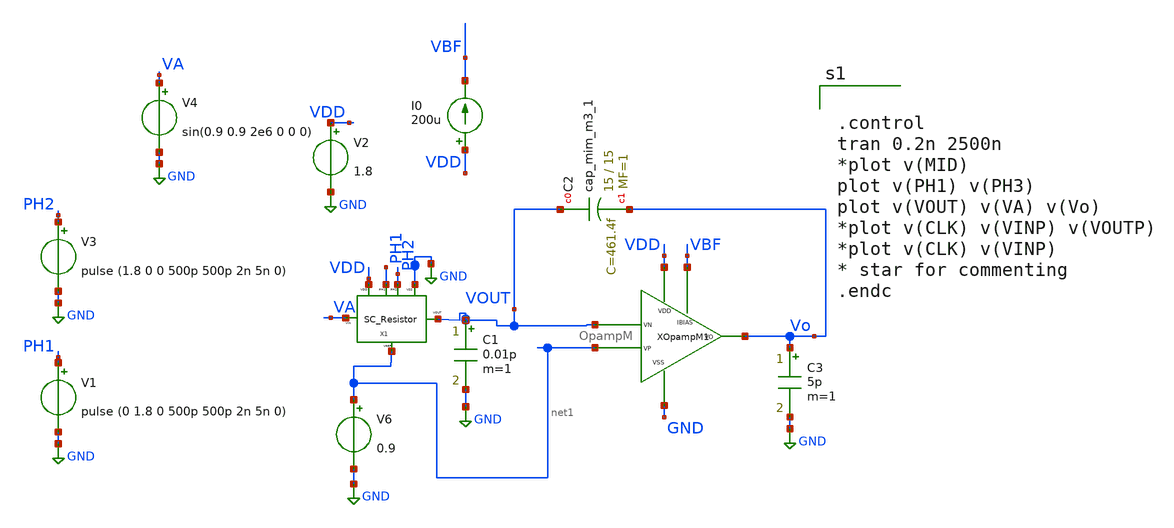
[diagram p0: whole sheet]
** sch_path: xschem/xschem_BGR_Top/Sigma_Delta/Integrator/Integrator_TB_rough.sch
**.subckt Integrator_TB_rough
V1 PH1 GND pulse (0 1.8 0 500p 500p 2n 5n 0)
V2 VDD GND 1.8
V3 PH2 GND pulse (1.8 0 0 500p 500p 2n 5n 0)
V6 net1 GND 0.9
C1 VOUT GND 0.01p m=1
X1 net1 PH2 VOUT VDD GND PH1 VA SC_Resistor
XOpampM1 VBF VDD VOUT net1 GND Vo OpampM
XC2 VOUT Vo sky130_fd_pr__cap_mim_m3_1 W=15 L=15 MF=1 m=1
I0 VDD VBF 200u
C3 Vo GND 5p m=1
V4 VA GND sin(0.9 0.9 2e6 0 0 0)
**** begin user architecture code


.control
tran 0.2n 2500n
*plot v(MID)
plot v(PH1) v(PH3)
plot v(VOUT) v(VA) v(Vo)
*plot v(CLK) v(VINP) v(VOUTP)
*plot v(CLK) v(VINP)
* star for commenting
.endc


** opencircuitdesign pdks install
.lib $::SKYWATER_MODELS/sky130.lib.spice tt


**** end user architecture code
**.ends

* expanding   symbol:  Sigma_Delta/SC_Resistor/SC_Resistor.sym # of pins=7
** sym_path: xschem/xschem_BGR_Top/Sigma_Delta/SC_Resistor/SC_Resistor.sym
** sch_path: xschem/xschem_BGR_Top/Sigma_Delta/SC_Resistor/SC_Resistor.sch
.subckt SC_Resistor VREF PH2 VOUT VDD VSS PH1 VIN
*.iopin VDD
*.iopin PH1
*.iopin VIN
*.iopin VOUT
*.iopin PH2
*.iopin VREF
*.iopin VSS
XTG3 VSS PH1 VDD VIN MID1 TG
XTG4 VSS PH2 VDD MID2 VOUT TG
XM2 MID1 PH2 VREF VSS sky130_fd_pr__nfet_01v8 L=0.15 W=20 nf=2 ad='int((nf+1)/2) * W/nf * 0.29' as='int((nf+2)/2) * W/nf * 0.29'
+ pd='2*int((nf+1)/2) * (W/nf + 0.29)' ps='2*int((nf+2)/2) * (W/nf + 0.29)' nrd='0.29 / W' nrs='0.29 / W'
+ sa=0 sb=0 sd=0 mult=1 m=1
XM1 MID2 PH1 VREF VSS sky130_fd_pr__nfet_01v8 L=0.15 W=20 nf=2 ad='int((nf+1)/2) * W/nf * 0.29' as='int((nf+2)/2) * W/nf * 0.29'
+ pd='2*int((nf+1)/2) * (W/nf + 0.29)' ps='2*int((nf+2)/2) * (W/nf + 0.29)' nrd='0.29 / W' nrs='0.29 / W'
+ sa=0 sb=0 sd=0 mult=1 m=1
XC2 MID2 MID1 sky130_fd_pr__cap_mim_m3_2 W=32 L=32 MF=1 m=1
.ends


* expanding   symbol:  Sigma_Delta/Op_Amp/OpampM.sym # of pins=6
** sym_path: xschem/xschem_BGR_Top/Op_Amp/OpampM.sym
** sch_path: xschem/xschem_BGR_Top/Op_Amp/OpampM.sch
.subckt OpampM IBIAS VDD VN VP VSS VO
*.iopin VDD
*.iopin VSS
*.iopin VP
*.iopin VN
*.iopin VO
*.iopin IBIAS
XM1 net1 VN net3 VSS sky130_fd_pr__nfet_01v8 L=0.5 W=50 nf=10 ad='int((nf+1)/2) * W/nf * 0.29' as='int((nf+2)/2) * W/nf * 0.29'
+ pd='2*int((nf+1)/2) * (W/nf + 0.29)' ps='2*int((nf+2)/2) * (W/nf + 0.29)' nrd='0.29 / W' nrs='0.29 / W'
+ sa=0 sb=0 sd=0 mult=1 m=1
XM3 net1 net1 VDD VDD sky130_fd_pr__pfet_01v8_lvt L=0.5 W=60 nf=10 ad='int((nf+1)/2) * W/nf * 0.29' as='int((nf+2)/2) * W/nf * 0.29'
+ pd='2*int((nf+1)/2) * (W/nf + 0.29)' ps='2*int((nf+2)/2) * (W/nf + 0.29)' nrd='0.29 / W' nrs='0.29 / W'
+ sa=0 sb=0 sd=0 mult=1 m=1
XM2 net2 VP net3 VSS sky130_fd_pr__nfet_01v8 L=0.5 W=50 nf=10 ad='int((nf+1)/2) * W/nf * 0.29' as='int((nf+2)/2) * W/nf * 0.29'
+ pd='2*int((nf+1)/2) * (W/nf + 0.29)' ps='2*int((nf+2)/2) * (W/nf + 0.29)' nrd='0.29 / W' nrs='0.29 / W'
+ sa=0 sb=0 sd=0 mult=1 m=1
XM4 net2 net1 VDD VDD sky130_fd_pr__pfet_01v8_lvt L=0.5 W=60 nf=10 ad='int((nf+1)/2) * W/nf * 0.29' as='int((nf+2)/2) * W/nf * 0.29'
+ pd='2*int((nf+1)/2) * (W/nf + 0.29)' ps='2*int((nf+2)/2) * (W/nf + 0.29)' nrd='0.29 / W' nrs='0.29 / W'
+ sa=0 sb=0 sd=0 mult=1 m=1
XM5 net3 IBIAS VSS VSS sky130_fd_pr__nfet_01v8 L=0.5 W=21 nf=10 ad='int((nf+1)/2) * W/nf * 0.29' as='int((nf+2)/2) * W/nf * 0.29'
+ pd='2*int((nf+1)/2) * (W/nf + 0.29)' ps='2*int((nf+2)/2) * (W/nf + 0.29)' nrd='0.29 / W' nrs='0.29 / W'
+ sa=0 sb=0 sd=0 mult=1 m=1
XM7 VO IBIAS VSS VSS sky130_fd_pr__nfet_01v8 L=0.5 W=63 nf=10 ad='int((nf+1)/2) * W/nf * 0.29' as='int((nf+2)/2) * W/nf * 0.29'
+ pd='2*int((nf+1)/2) * (W/nf + 0.29)' ps='2*int((nf+2)/2) * (W/nf + 0.29)' nrd='0.29 / W' nrs='0.29 / W'
+ sa=0 sb=0 sd=0 mult=1 m=1
XM8 IBIAS IBIAS VSS VSS sky130_fd_pr__nfet_01v8 L=0.5 W=21 nf=10 ad='int((nf+1)/2) * W/nf * 0.29' as='int((nf+2)/2) * W/nf * 0.29'
+ pd='2*int((nf+1)/2) * (W/nf + 0.29)' ps='2*int((nf+2)/2) * (W/nf + 0.29)' nrd='0.29 / W' nrs='0.29 / W'
+ sa=0 sb=0 sd=0 mult=1 m=1
XC1 net2 VO sky130_fd_pr__cap_mim_m3_1 W=24 L=24 MF=1 m=1
XC2 VDD VSS sky130_fd_pr__cap_mim_m3_1 W=30 L=10 MF=1 m=1
XC3 VDD VSS sky130_fd_pr__cap_mim_m3_1 W=30 L=10 MF=1 m=1
XM6 VO net2 VDD VDD sky130_fd_pr__pfet_01v8_lvt L=0.50 W=355 nf=20 ad='int((nf+1)/2) * W/nf * 0.29' as='int((nf+2)/2) * W/nf * 0.29'
+ pd='2*int((nf+1)/2) * (W/nf + 0.29)' ps='2*int((nf+2)/2) * (W/nf + 0.29)' nrd='0.29 / W' nrs='0.29 / W'
+ sa=0 sb=0 sd=0 mult=1 m=1
.ends


* expanding   symbol:  Sigma_Delta/Transmission_Gate/TG.sym # of pins=5
** sym_path: xschem/xschem_BGR_Top/Sigma_Delta/Transmission_Gate/TG.sym
** sch_path: xschem/xschem_BGR_Top/Sigma_Delta/Transmission_Gate/TG.sch
.subckt TG VSS CLK VDD A B
*.iopin VDD
*.iopin VSS
*.iopin A
*.iopin B
*.iopin CLK
XM1 A CLK B VSS sky130_fd_pr__nfet_01v8 L=0.15 W=10 nf=1 ad='int((nf+1)/2) * W/nf * 0.29' as='int((nf+2)/2) * W/nf * 0.29'
+ pd='2*int((nf+1)/2) * (W/nf + 0.29)' ps='2*int((nf+2)/2) * (W/nf + 0.29)' nrd='0.29 / W' nrs='0.29 / W'
+ sa=0 sb=0 sd=0 mult=1 m=1
XM2 B CLKB A VDD sky130_fd_pr__pfet_01v8 L=0.15 W=20 nf=2 ad='int((nf+1)/2) * W/nf * 0.29' as='int((nf+2)/2) * W/nf * 0.29'
+ pd='2*int((nf+1)/2) * (W/nf + 0.29)' ps='2*int((nf+2)/2) * (W/nf + 0.29)' nrd='0.29 / W' nrs='0.29 / W'
+ sa=0 sb=0 sd=0 mult=1 m=1
XM3 CLKB CLK VSS VSS sky130_fd_pr__nfet_01v8 L=0.15 W=10 nf=5 ad='int((nf+1)/2) * W/nf * 0.29' as='int((nf+2)/2) * W/nf * 0.29'
+ pd='2*int((nf+1)/2) * (W/nf + 0.29)' ps='2*int((nf+2)/2) * (W/nf + 0.29)' nrd='0.29 / W' nrs='0.29 / W'
+ sa=0 sb=0 sd=0 mult=1 m=1
XM4 CLKB CLK VDD VDD sky130_fd_pr__pfet_01v8 L=0.15 W=20 nf=10 ad='int((nf+1)/2) * W/nf * 0.29' as='int((nf+2)/2) * W/nf * 0.29'
+ pd='2*int((nf+1)/2) * (W/nf + 0.29)' ps='2*int((nf+2)/2) * (W/nf + 0.29)' nrd='0.29 / W' nrs='0.29 / W'
+ sa=0 sb=0 sd=0 mult=1 m=1
.ends

.GLOBAL GND
.end
